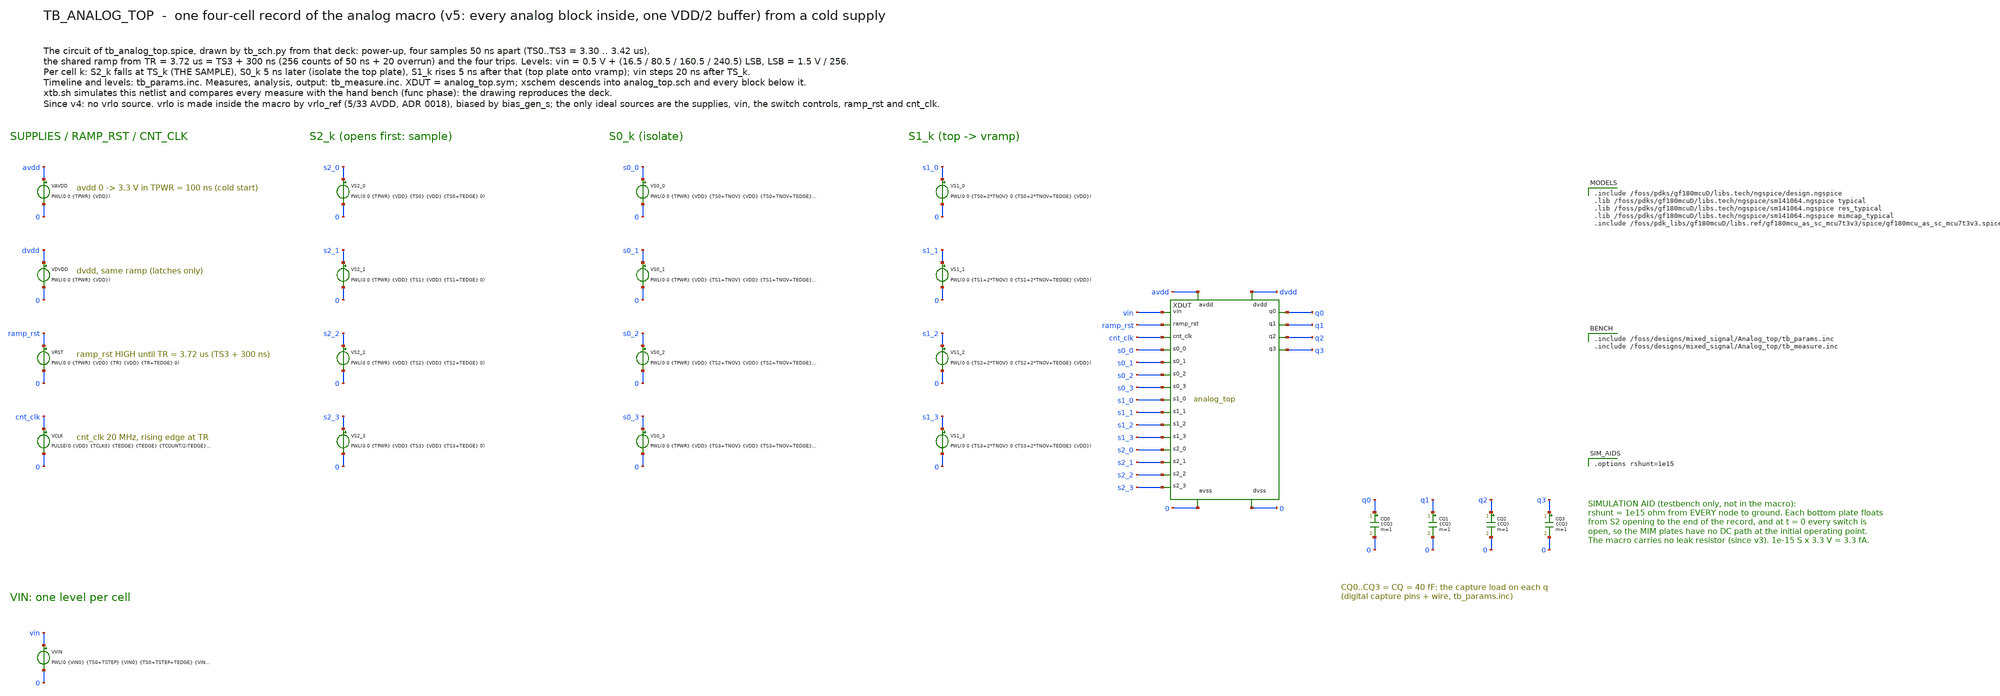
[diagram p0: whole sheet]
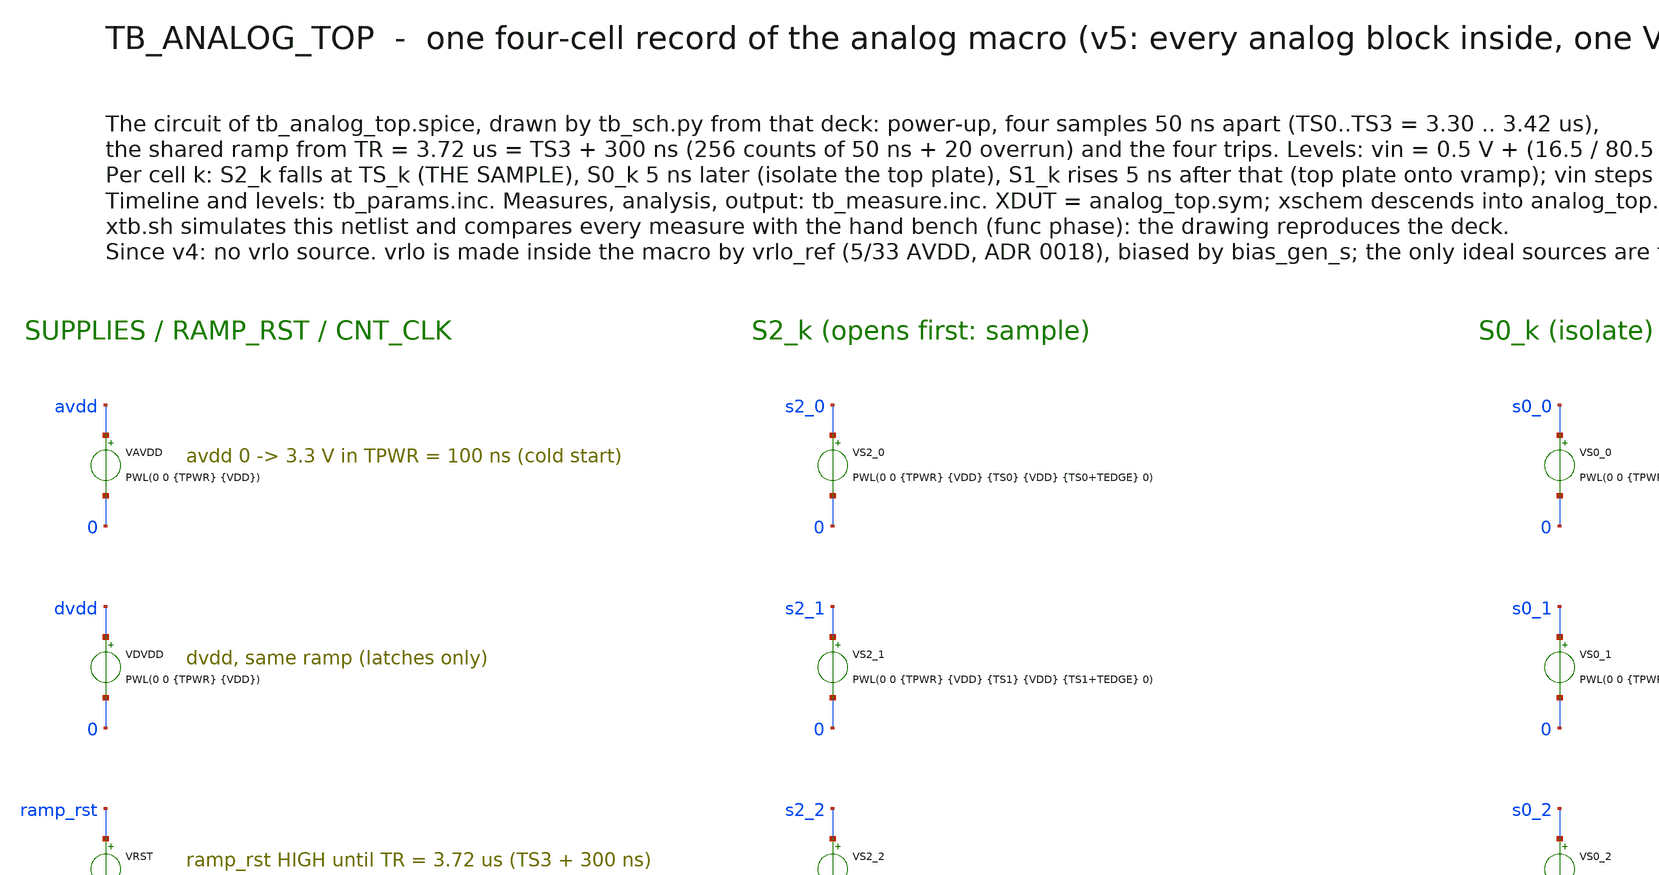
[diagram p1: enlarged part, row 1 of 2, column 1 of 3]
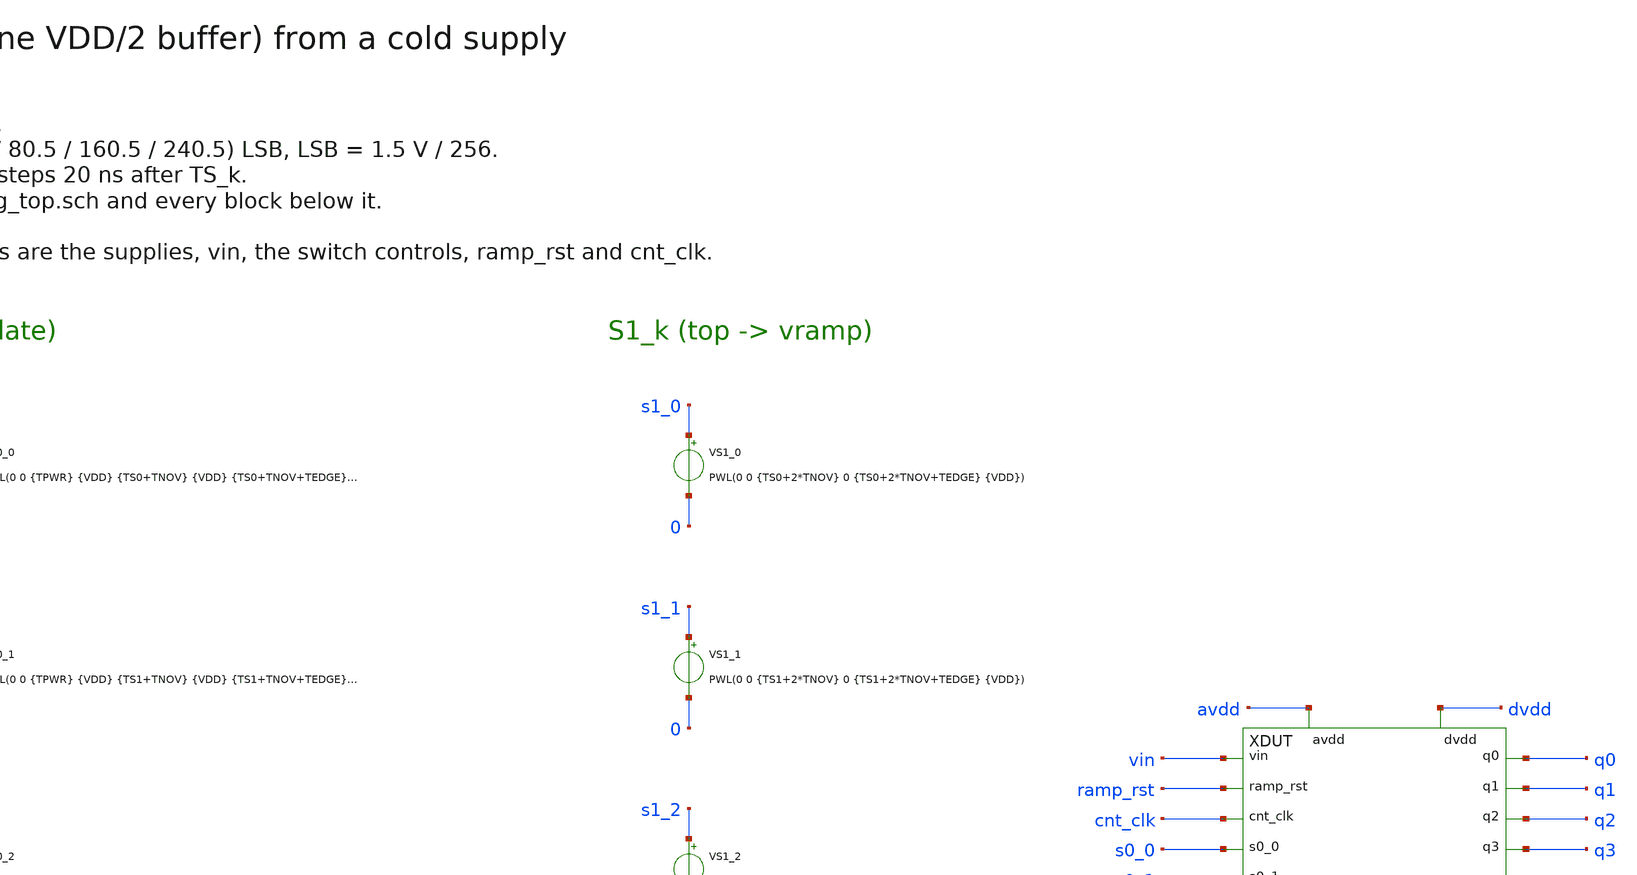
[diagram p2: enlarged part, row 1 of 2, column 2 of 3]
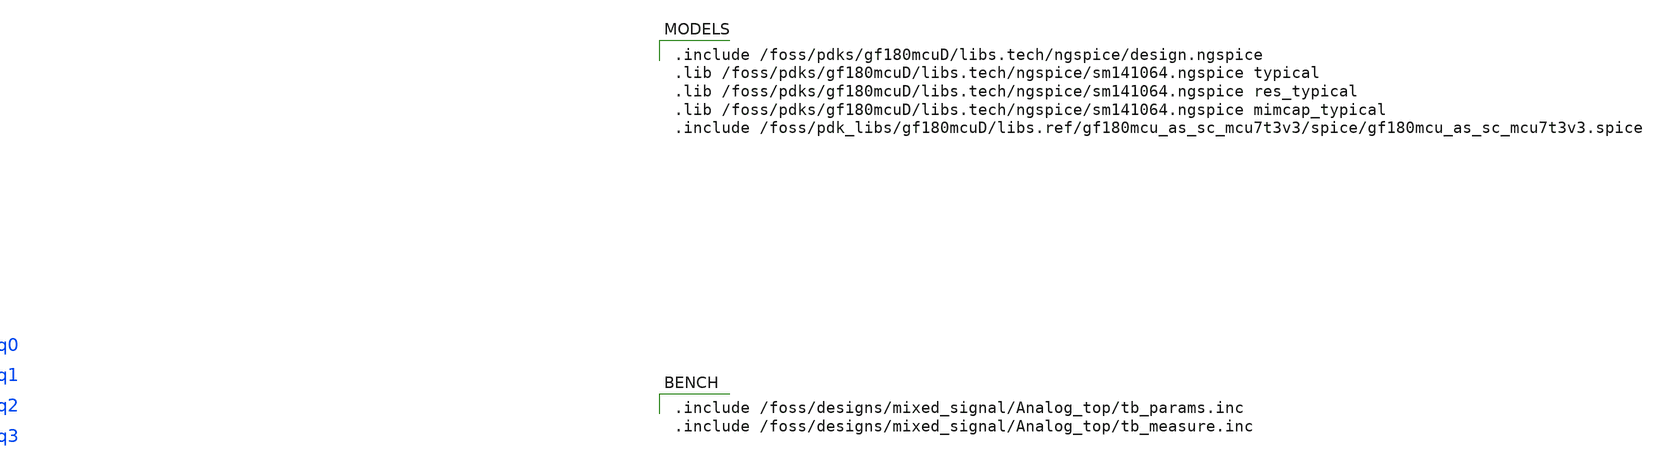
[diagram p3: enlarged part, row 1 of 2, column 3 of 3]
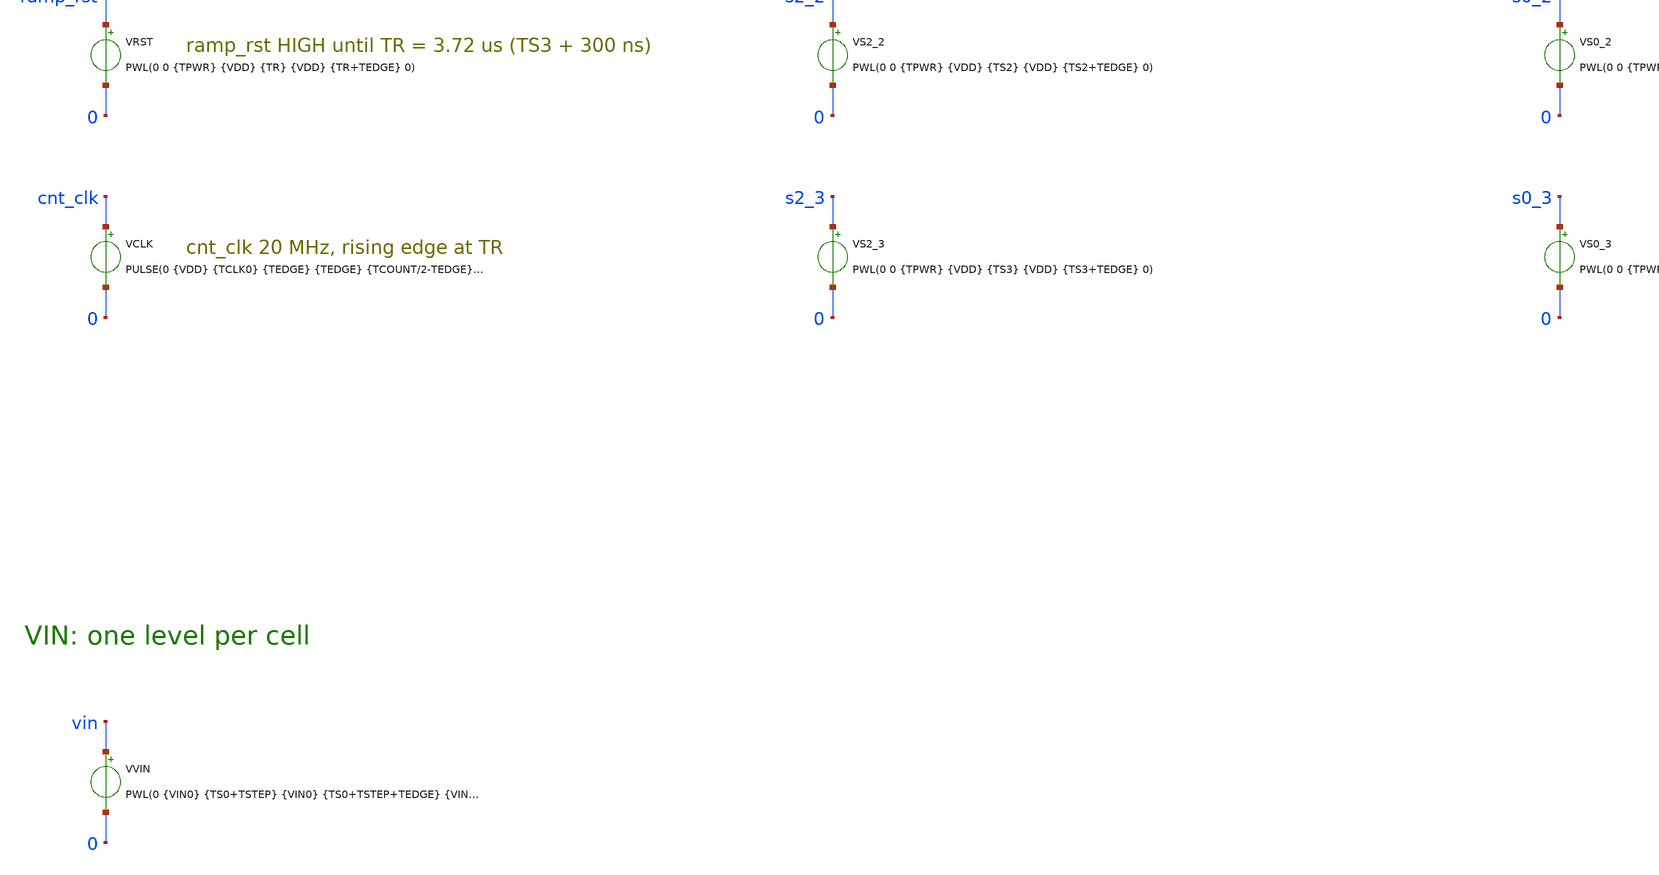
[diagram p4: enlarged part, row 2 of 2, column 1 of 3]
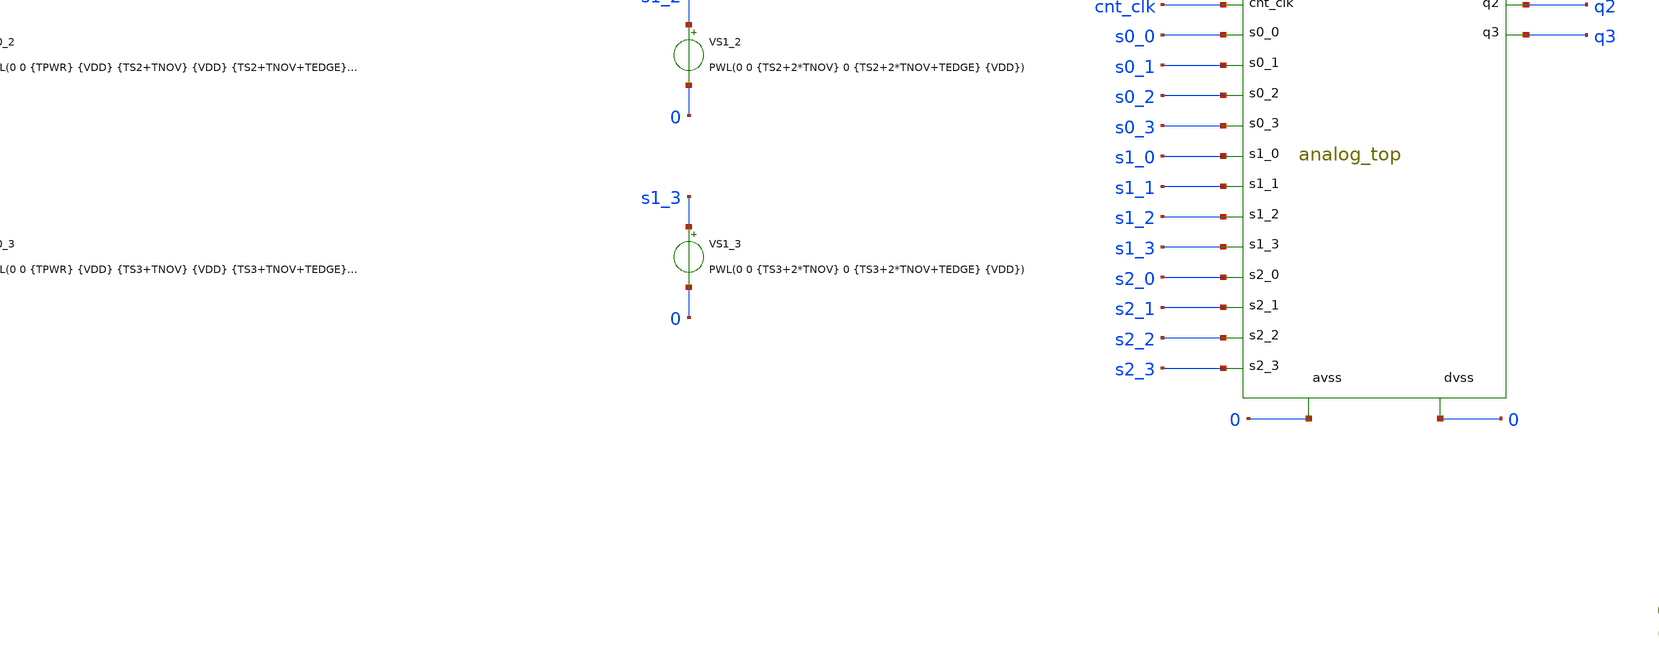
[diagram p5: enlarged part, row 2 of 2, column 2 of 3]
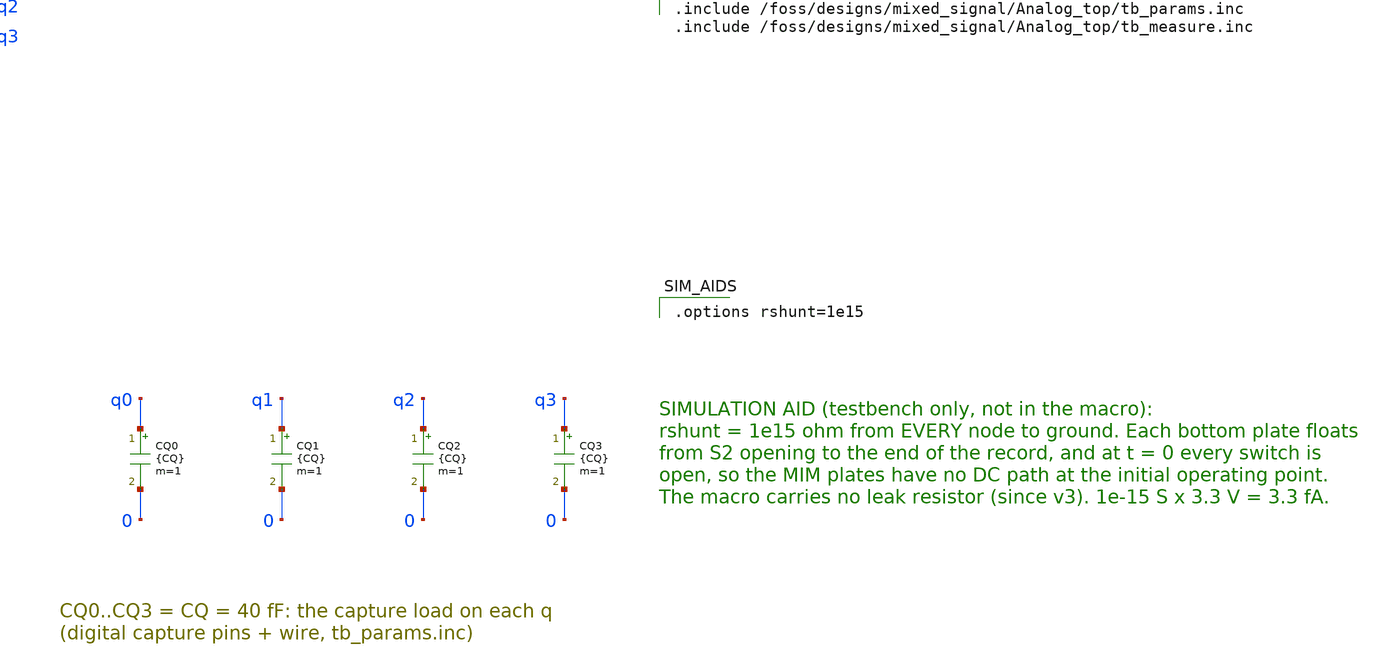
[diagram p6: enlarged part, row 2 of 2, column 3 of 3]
** sch_path: mixed_signal/Analog_top/tb_analog_top.sch
**.subckt tb_analog_top
VAVDD avdd 0 PWL(0 0 {TPWR} {VDD})
VDVDD dvdd 0 PWL(0 0 {TPWR} {VDD})
VRST ramp_rst 0 PWL(0 0 {TPWR} {VDD} {TR} {VDD} {TR+TEDGE} 0)
VCLK cnt_clk 0 PULSE(0 {VDD} {TCLK0} {TEDGE} {TEDGE} {TCOUNT/2-TEDGE} {TCOUNT})
VS2_0 s2_0 0 PWL(0 0 {TPWR} {VDD} {TS0} {VDD} {TS0+TEDGE} 0)
VS2_1 s2_1 0 PWL(0 0 {TPWR} {VDD} {TS1} {VDD} {TS1+TEDGE} 0)
VS2_2 s2_2 0 PWL(0 0 {TPWR} {VDD} {TS2} {VDD} {TS2+TEDGE} 0)
VS2_3 s2_3 0 PWL(0 0 {TPWR} {VDD} {TS3} {VDD} {TS3+TEDGE} 0)
VS0_0 s0_0 0 PWL(0 0 {TPWR} {VDD} {TS0+TNOV} {VDD} {TS0+TNOV+TEDGE} 0)
VS0_1 s0_1 0 PWL(0 0 {TPWR} {VDD} {TS1+TNOV} {VDD} {TS1+TNOV+TEDGE} 0)
VS0_2 s0_2 0 PWL(0 0 {TPWR} {VDD} {TS2+TNOV} {VDD} {TS2+TNOV+TEDGE} 0)
VS0_3 s0_3 0 PWL(0 0 {TPWR} {VDD} {TS3+TNOV} {VDD} {TS3+TNOV+TEDGE} 0)
VS1_0 s1_0 0 PWL(0 0 {TS0+2*TNOV} 0 {TS0+2*TNOV+TEDGE} {VDD})
VS1_1 s1_1 0 PWL(0 0 {TS1+2*TNOV} 0 {TS1+2*TNOV+TEDGE} {VDD})
VS1_2 s1_2 0 PWL(0 0 {TS2+2*TNOV} 0 {TS2+2*TNOV+TEDGE} {VDD})
VS1_3 s1_3 0 PWL(0 0 {TS3+2*TNOV} 0 {TS3+2*TNOV+TEDGE} {VDD})
VVIN vin 0 PWL(0 {VIN0} {TS0+TSTEP} {VIN0} {TS0+TSTEP+TEDGE} {VIN1} {TS1+TSTEP} {VIN1} {TS1+TSTEP+TEDGE}
+ {VIN2} {TS2+TSTEP} {VIN2} {TS2+TSTEP+TEDGE} {VIN3})
XDUT vin ramp_rst cnt_clk s0_0 s0_1 s0_2 s0_3 s1_0 s1_1 s1_2 s1_3 s2_0 s2_1 s2_2 s2_3 q0 q1 q2 q3
+ avdd 0 dvdd 0 analog_top
CQ0 q0 0 {CQ} m=1
CQ1 q1 0 {CQ} m=1
CQ2 q2 0 {CQ} m=1
CQ3 q3 0 {CQ} m=1
**** begin user architecture code

.include /foss/pdks/gf180mcuD/libs.tech/ngspice/design.ngspice
.lib /foss/pdks/gf180mcuD/libs.tech/ngspice/sm141064.ngspice typical
.lib /foss/pdks/gf180mcuD/libs.tech/ngspice/sm141064.ngspice res_typical
.lib /foss/pdks/gf180mcuD/libs.tech/ngspice/sm141064.ngspice mimcap_typical
.include /foss/pdk_libs/gf180mcuD/libs.ref/gf180mcu_as_sc_mcu7t3v3/spice/gf180mcu_as_sc_mcu7t3v3.spice


.include /foss/designs/mixed_signal/Analog_top/tb_params.inc
.include /foss/designs/mixed_signal/Analog_top/tb_measure.inc


.options rshunt=1e15

**** end user architecture code
**.ends
.end
